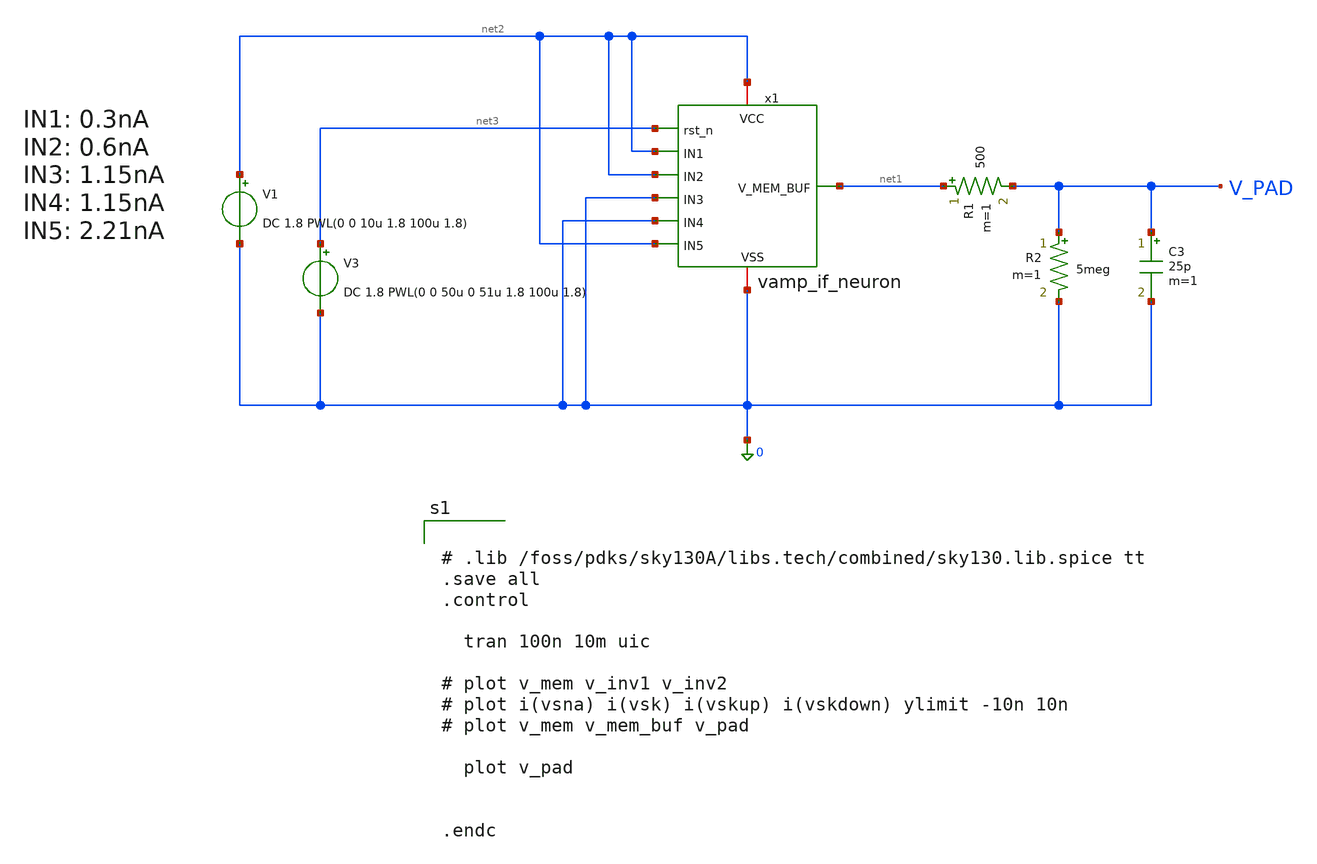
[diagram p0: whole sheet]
** sch_path: schem/vamp_if_neuron_tb.sch
**.subckt vamp_if_neuron_tb
V1 net2 0 DC 1.8 PWL(0 0 10u 1.8 100u 1.8)
V3 net3 0 DC 1.8 PWL(0 0 50u 0 51u 1.8 100u 1.8)
R1 net1 V_PAD 500 m=1
R2 V_PAD 0 5meg m=1
C3 V_PAD 0 25p m=1
x1 net2 net1 0 net3 net2 net2 0 0 net2 vamp_if_neuron
**** begin user architecture code


# .lib /foss/pdks/sky130A/libs.tech/combined/sky130.lib.spice tt
.save all
.control

  tran 100n 10m uic

# plot v_mem v_inv1 v_inv2
# plot i(vsna) i(vsk) i(vskup) i(vskdown) ylimit -10n 10n
# plot v_mem v_mem_buf v_pad

  plot v_pad


.endc



** opencircuitdesign pdks install
.lib $::SKYWATER_MODELS/sky130.lib.spice tt

**** end user architecture code
**.ends

* expanding   symbol:  vamp_if_neuron.sym # of pins=9
** sym_path: schem/vamp_if_neuron.sym
** sch_path: schem/vamp_if_neuron.sch
.subckt vamp_if_neuron VCC V_MEM_BUF VSS rst_n IN1 IN2 IN3 IN4 IN5
*.iopin VCC
*.iopin VSS
*.ipin rst_n
*.opin V_MEM_BUF
*.ipin IN1
*.ipin IN2
*.ipin IN3
*.ipin IN4
*.ipin IN5
x1 VCC net1 VSS VBN_REF10N V_MEM V_THRES ota
x2 VCC net1 V_inv1 VSS inv
XC1 V_MEM VSS sky130_fd_pr__cap_mim_m3_1 W=32 L=32 MF=1 m=1
XM1 net5 V_inv2 VK_SRC VSS sky130_fd_pr__nfet_01v8 L=4 W=1 nf=1 ad='int((1 + 1)/2) * 1 / 1 * 0.29' as='int((1 + 2)/2) * 1 / 1 * 0.29'
+ pd='2*int((1 + 1)/2) * (1 / 1 + 0.29)' ps='2*int((1 + 2)/2) * (1 / 1 + 0.29)' nrd='0.29 / 1 ' nrs='0.29 / 1 '
+ sa=0 sb=0 sd=0 mult=1 m=1
XM5 V_inv2 V_inv1 VNET_KDOWN_SRC VSS sky130_fd_pr__nfet_01v8 L=0.5 W=1 nf=1 ad='int((1 + 1)/2) * 1 / 1 * 0.29'
+ as='int((1 + 2)/2) * 1 / 1 * 0.29' pd='2*int((1 + 1)/2) * (1 / 1 + 0.29)' ps='2*int((1 + 2)/2) * (1 / 1 + 0.29)'
+ nrd='0.29 / 1 ' nrs='0.29 / 1 ' sa=0 sb=0 sd=0 mult=1 m=1
XM6 V_inv2 V_inv1 net3 VCC sky130_fd_pr__pfet_01v8_lvt L=0.5 W=2 nf=1 ad='int((1 + 1)/2) * 2 / 1 * 0.29'
+ as='int((1 + 2)/2) * 2 / 1 * 0.29' pd='2*int((1 + 1)/2) * (2 / 1 + 0.29)' ps='2*int((1 + 2)/2) * (2 / 1 + 0.29)'
+ nrd='0.29 / 2 ' nrs='0.29 / 2 ' sa=0 sb=0 sd=0 mult=1 m=1
XC2 V_inv2 VSS sky130_fd_pr__cap_mim_m3_1 W=35 L=35 MF=1 m=1
VSNA net6 V_MEM 0
.save i(vsna)
VSKUP net4 net3 0
.save i(vskup)
VSK net5 V_MEM 0
.save i(vsk)
VSKDOWN net2 VNET_KDOWN_SRC 0
.save i(vskdown)
XM2 VK_SRC VBN_REF10N VSS VSS sky130_fd_pr__nfet_01v8 L=4 W=1 nf=1 ad='int((1 + 1)/2) * 1 / 1 * 0.29'
+ as='int((1 + 2)/2) * 1 / 1 * 0.29' pd='2*int((1 + 1)/2) * (1 / 1 + 0.29)' ps='2*int((1 + 2)/2) * (1 / 1 + 0.29)'
+ nrd='0.29 / 1 ' nrs='0.29 / 1 ' sa=0 sb=0 sd=0 mult=4 m=4
XM3 net2 VBN_REF1N VSS VSS sky130_fd_pr__nfet_01v8 L=4 W=2 nf=1 ad='int((1 + 1)/2) * 2 / 1 * 0.29' as='int((1 + 2)/2) * 2 / 1 * 0.29'
+ pd='2*int((1 + 1)/2) * (2 / 1 + 0.29)' ps='2*int((1 + 2)/2) * (2 / 1 + 0.29)' nrd='0.29 / 2 ' nrs='0.29 / 2 '
+ sa=0 sb=0 sd=0 mult=1 m=1
XM7 VNA_SRC VBP_REF10N VCC VCC sky130_fd_pr__pfet_01v8 L=4 W=1 nf=1 ad='int((1 + 1)/2) * 1 / 1 * 0.29'
+ as='int((1 + 2)/2) * 1 / 1 * 0.29' pd='2*int((1 + 1)/2) * (1 / 1 + 0.29)' ps='2*int((1 + 2)/2) * (1 / 1 + 0.29)'
+ nrd='0.29 / 1 ' nrs='0.29 / 1 ' sa=0 sb=0 sd=0 mult=1 m=1
XM8 net4 VBP_REF1N VCC VCC sky130_fd_pr__pfet_01v8 L=4 W=2.5 nf=1 ad='int((1 + 1)/2) * 2.5 / 1 * 0.29'
+ as='int((1 + 2)/2) * 2.5 / 1 * 0.29' pd='2*int((1 + 1)/2) * (2.5 / 1 + 0.29)' ps='2*int((1 + 2)/2) * (2.5 / 1 + 0.29)'
+ nrd='0.29 / 2.5 ' nrs='0.29 / 2.5 ' sa=0 sb=0 sd=0 mult=2 m=2
XM4 net6 V_inv1 VNA_SRC VCC sky130_fd_pr__pfet_01v8_lvt L=4 W=2 nf=1 ad='int((1 + 1)/2) * 2 / 1 * 0.29'
+ as='int((1 + 2)/2) * 2 / 1 * 0.29' pd='2*int((1 + 1)/2) * (2 / 1 + 0.29)' ps='2*int((1 + 2)/2) * (2 / 1 + 0.29)'
+ nrd='0.29 / 2 ' nrs='0.29 / 2 ' sa=0 sb=0 sd=0 mult=1 m=1
VSIN V_STIM V_MEM 0
.save i(vsin)
x3 VCC VBP_REF10N VSS VBP_REF1N VBN_REF10N VBN_REF1N rst_n bmr
VSBUF net7 V_MEM_BUF 0
.save i(vsbuf)
XM9 VSS V_MEM V_MEM_BUF VCC sky130_fd_pr__pfet_01v8_lvt L=0.5 W=40 nf=1 ad='int((1 + 1)/2) * 40 / 1 * 0.29'
+ as='int((1 + 2)/2) * 40 / 1 * 0.29' pd='2*int((1 + 1)/2) * (40 / 1 + 0.29)' ps='2*int((1 + 2)/2) * (40 / 1 + 0.29)'
+ nrd='0.29 / 40 ' nrs='0.29 / 40 ' sa=0 sb=0 sd=0 mult=1 m=1
XM10 net7 VBP_REF10N VCC VCC sky130_fd_pr__pfet_01v8 L=0.75 W=10 nf=5 ad='int((5 + 1)/2) * 10 / 5 * 0.29'
+ as='int((5 + 2)/2) * 10 / 5 * 0.29' pd='2*int((5 + 1)/2) * (10 / 5 + 0.29)' ps='2*int((5 + 2)/2) * (10 / 5 + 0.29)'
+ nrd='0.29 / 10 ' nrs='0.29 / 10 ' sa=0 sb=0 sd=0 mult=2 m=2
XM11 net8 VBN_REF1N VSS VSS sky130_fd_pr__nfet_01v8 L=4 W=1 nf=1 ad='int((1 + 1)/2) * 1 / 1 * 0.29' as='int((1 + 2)/2) * 1 / 1 * 0.29'
+ pd='2*int((1 + 1)/2) * (1 / 1 + 0.29)' ps='2*int((1 + 2)/2) * (1 / 1 + 0.29)' nrd='0.29 / 1 ' nrs='0.29 / 1 '
+ sa=0 sb=0 sd=0 mult=1 m=1
VSLK net8 V_MEM 0
.save i(vslk)
X0.5 net9 VBP_REF1N VCC VCC sky130_fd_pr__pfet_01v8 L=16 W=0.5 nf=1 ad='int((1 + 1)/2) * 0.5 / 1 * 0.29'
+ as='int((1 + 2)/2) * 0.5 / 1 * 0.29' pd='2*int((1 + 1)/2) * (0.5 / 1 + 0.29)' ps='2*int((1 + 2)/2) * (0.5 / 1 + 0.29)'
+ nrd='0.29 / 0.5 ' nrs='0.29 / 0.5 ' sa=0 sb=0 sd=0 mult=1 m=1
XM13 V_STIM IN1 net9 VCC sky130_fd_pr__pfet_01v8_lvt L=4 W=2 nf=1 ad='int((1 + 1)/2) * 2 / 1 * 0.29'
+ as='int((1 + 2)/2) * 2 / 1 * 0.29' pd='2*int((1 + 1)/2) * (2 / 1 + 0.29)' ps='2*int((1 + 2)/2) * (2 / 1 + 0.29)'
+ nrd='0.29 / 2 ' nrs='0.29 / 2 ' sa=0 sb=0 sd=0 mult=1 m=1
XM14 net10 VBP_REF1N VCC VCC sky130_fd_pr__pfet_01v8 L=8 W=0.5 nf=1 ad='int((1 + 1)/2) * 0.5 / 1 * 0.29'
+ as='int((1 + 2)/2) * 0.5 / 1 * 0.29' pd='2*int((1 + 1)/2) * (0.5 / 1 + 0.29)' ps='2*int((1 + 2)/2) * (0.5 / 1 + 0.29)'
+ nrd='0.29 / 0.5 ' nrs='0.29 / 0.5 ' sa=0 sb=0 sd=0 mult=1 m=1
XM15 V_STIM IN2 net10 VCC sky130_fd_pr__pfet_01v8_lvt L=4 W=2 nf=1 ad='int((1 + 1)/2) * 2 / 1 * 0.29'
+ as='int((1 + 2)/2) * 2 / 1 * 0.29' pd='2*int((1 + 1)/2) * (2 / 1 + 0.29)' ps='2*int((1 + 2)/2) * (2 / 1 + 0.29)'
+ nrd='0.29 / 2 ' nrs='0.29 / 2 ' sa=0 sb=0 sd=0 mult=1 m=1
XM16 net11 VBP_REF1N VCC VCC sky130_fd_pr__pfet_01v8 L=4 W=1 nf=1 ad='int((1 + 1)/2) * 1 / 1 * 0.29'
+ as='int((1 + 2)/2) * 1 / 1 * 0.29' pd='2*int((1 + 1)/2) * (1 / 1 + 0.29)' ps='2*int((1 + 2)/2) * (1 / 1 + 0.29)'
+ nrd='0.29 / 1 ' nrs='0.29 / 1 ' sa=0 sb=0 sd=0 mult=1 m=1
XM17 V_STIM IN3 net11 VCC sky130_fd_pr__pfet_01v8_lvt L=4 W=2 nf=1 ad='int((1 + 1)/2) * 2 / 1 * 0.29'
+ as='int((1 + 2)/2) * 2 / 1 * 0.29' pd='2*int((1 + 1)/2) * (2 / 1 + 0.29)' ps='2*int((1 + 2)/2) * (2 / 1 + 0.29)'
+ nrd='0.29 / 2 ' nrs='0.29 / 2 ' sa=0 sb=0 sd=0 mult=1 m=1
XM18 net12 VBP_REF1N VCC VCC sky130_fd_pr__pfet_01v8 L=4 W=1 nf=1 ad='int((1 + 1)/2) * 1 / 1 * 0.29'
+ as='int((1 + 2)/2) * 1 / 1 * 0.29' pd='2*int((1 + 1)/2) * (1 / 1 + 0.29)' ps='2*int((1 + 2)/2) * (1 / 1 + 0.29)'
+ nrd='0.29 / 1 ' nrs='0.29 / 1 ' sa=0 sb=0 sd=0 mult=1 m=1
XM19 V_STIM IN4 net12 VCC sky130_fd_pr__pfet_01v8_lvt L=4 W=2 nf=1 ad='int((1 + 1)/2) * 2 / 1 * 0.29'
+ as='int((1 + 2)/2) * 2 / 1 * 0.29' pd='2*int((1 + 1)/2) * (2 / 1 + 0.29)' ps='2*int((1 + 2)/2) * (2 / 1 + 0.29)'
+ nrd='0.29 / 2 ' nrs='0.29 / 2 ' sa=0 sb=0 sd=0 mult=1 m=1
XM20 net13 VBP_REF1N VCC VCC sky130_fd_pr__pfet_01v8 L=4 W=1 nf=1 ad='int((1 + 1)/2) * 1 / 1 * 0.29'
+ as='int((1 + 2)/2) * 1 / 1 * 0.29' pd='2*int((1 + 1)/2) * (1 / 1 + 0.29)' ps='2*int((1 + 2)/2) * (1 / 1 + 0.29)'
+ nrd='0.29 / 1 ' nrs='0.29 / 1 ' sa=0 sb=0 sd=0 mult=2 m=2
XM21 V_STIM IN5 net13 VCC sky130_fd_pr__pfet_01v8_lvt L=4 W=2 nf=1 ad='int((1 + 1)/2) * 2 / 1 * 0.29'
+ as='int((1 + 2)/2) * 2 / 1 * 0.29' pd='2*int((1 + 1)/2) * (2 / 1 + 0.29)' ps='2*int((1 + 2)/2) * (2 / 1 + 0.29)'
+ nrd='0.29 / 2 ' nrs='0.29 / 2 ' sa=0 sb=0 sd=0 mult=1 m=1
XR3 V_THRES VCC VSS sky130_fd_pr__res_xhigh_po_0p35 L=10 mult=1 m=1
XR4 VSS V_THRES VSS sky130_fd_pr__res_xhigh_po_0p35 L=6.36 mult=1 m=1
.ends


* expanding   symbol:  ota/ota.sym # of pins=6
** sym_path: schem/ota/ota.sym
** sch_path: schem/ota/ota.sch
.subckt ota VCC OUT VSS BIAS + -
*.ipin BIAS
*.ipin +
*.ipin -
*.opin OUT
*.iopin VCC
*.iopin VSS
XM1 VSRC + VBOT VSS sky130_fd_pr__nfet_01v8 L=0.5 W=1 nf=1 ad='int((1 + 1)/2) * 1 / 1 * 0.29' as='int((1 + 2)/2) * 1 / 1 * 0.29'
+ pd='2*int((1 + 1)/2) * (1 / 1 + 0.29)' ps='2*int((1 + 2)/2) * (1 / 1 + 0.29)' nrd='0.29 / 1 ' nrs='0.29 / 1 '
+ sa=0 sb=0 sd=0 mult=1 m=1
XM2 OUT - VBOT VSS sky130_fd_pr__nfet_01v8 L=0.5 W=1 nf=1 ad='int((1 + 1)/2) * 1 / 1 * 0.29' as='int((1 + 2)/2) * 1 / 1 * 0.29'
+ pd='2*int((1 + 1)/2) * (1 / 1 + 0.29)' ps='2*int((1 + 2)/2) * (1 / 1 + 0.29)' nrd='0.29 / 1 ' nrs='0.29 / 1 '
+ sa=0 sb=0 sd=0 mult=1 m=1
XM3 VSRC VSRC VCC VCC sky130_fd_pr__pfet_01v8_lvt L=0.5 W=2 nf=1 ad='int((1 + 1)/2) * 2 / 1 * 0.29' as='int((1 + 2)/2) * 2 / 1 * 0.29'
+ pd='2*int((1 + 1)/2) * (2 / 1 + 0.29)' ps='2*int((1 + 2)/2) * (2 / 1 + 0.29)' nrd='0.29 / 2 ' nrs='0.29 / 2 '
+ sa=0 sb=0 sd=0 mult=1 m=1
XM4 OUT VSRC VCC VCC sky130_fd_pr__pfet_01v8_lvt L=0.5 W=2 nf=1 ad='int((1 + 1)/2) * 2 / 1 * 0.29' as='int((1 + 2)/2) * 2 / 1 * 0.29'
+ pd='2*int((1 + 1)/2) * (2 / 1 + 0.29)' ps='2*int((1 + 2)/2) * (2 / 1 + 0.29)' nrd='0.29 / 2 ' nrs='0.29 / 2 '
+ sa=0 sb=0 sd=0 mult=1 m=1
XM5 VBOT BIAS VSS VSS sky130_fd_pr__nfet_01v8 L=0.5 W=1 nf=1 ad='int((1 + 1)/2) * 1 / 1 * 0.29' as='int((1 + 2)/2) * 1 / 1 * 0.29'
+ pd='2*int((1 + 1)/2) * (1 / 1 + 0.29)' ps='2*int((1 + 2)/2) * (1 / 1 + 0.29)' nrd='0.29 / 1 ' nrs='0.29 / 1 '
+ sa=0 sb=0 sd=0 mult=1 m=1
.ends


* expanding   symbol:  inv/inv.sym # of pins=4
** sym_path: schem/inv/inv.sym
** sch_path: schem/inv/inv.sch
.subckt inv VDD IN OUT VSS
*.ipin IN
*.iopin VDD
*.iopin VSS
*.opin OUT
XM1 OUT IN VSS VSS sky130_fd_pr__nfet_01v8 L=0.5 W=1 nf=1 ad='int((1 + 1)/2) * 1 / 1 * 0.29' as='int((1 + 2)/2) * 1 / 1 * 0.29'
+ pd='2*int((1 + 1)/2) * (1 / 1 + 0.29)' ps='2*int((1 + 2)/2) * (1 / 1 + 0.29)' nrd='0.29 / 1 ' nrs='0.29 / 1 '
+ sa=0 sb=0 sd=0 mult=1 m=1
XM2 OUT IN VDD VDD sky130_fd_pr__pfet_01v8_lvt L=0.5 W=2 nf=1 ad='int((1 + 1)/2) * 2 / 1 * 0.29' as='int((1 + 2)/2) * 2 / 1 * 0.29'
+ pd='2*int((1 + 1)/2) * (2 / 1 + 0.29)' ps='2*int((1 + 2)/2) * (2 / 1 + 0.29)' nrd='0.29 / 2 ' nrs='0.29 / 2 '
+ sa=0 sb=0 sd=0 mult=1 m=1
.ends


* expanding   symbol:  bias/bmr.sym # of pins=7
** sym_path: schem/bias/bmr.sym
** sch_path: schem/bias/bmr.sch
.subckt bmr VCC VBP_REF10N VSS VBP_REF1N VBN_REF10N VBN_REF1N rst_n
*.iopin VCC
*.iopin VSS
*.ipin rst_n
*.opin VBP_REF10N
*.opin VBP_REF1N
*.opin VBN_REF10N
*.opin VBN_REF1N
x1 VCC VBP_REF10N VSS VBN_REF10N rst_n bmr_10n
XM1 net1 VBP_REF10N VCC VCC sky130_fd_pr__pfet_01v8 L=4 W=1 nf=1 ad='int((1 + 1)/2) * 1 / 1 * 0.29' as='int((1 + 2)/2) * 1 / 1 * 0.29'
+ pd='2*int((1 + 1)/2) * (1 / 1 + 0.29)' ps='2*int((1 + 2)/2) * (1 / 1 + 0.29)' nrd='0.29 / 1 ' nrs='0.29 / 1 '
+ sa=0 sb=0 sd=0 mult=1 m=1
XM2 VBN_REF1N VBN_REF1N VSS VSS sky130_fd_pr__nfet_01v8 L=4 W=1 nf=1 ad='int((1 + 1)/2) * 1 / 1 * 0.29'
+ as='int((1 + 2)/2) * 1 / 1 * 0.29' pd='2*int((1 + 1)/2) * (1 / 1 + 0.29)' ps='2*int((1 + 2)/2) * (1 / 1 + 0.29)'
+ nrd='0.29 / 1 ' nrs='0.29 / 1 ' sa=0 sb=0 sd=0 mult=10 m=10
XM3 net2 VBN_REF1N VSS VSS sky130_fd_pr__nfet_01v8 L=4 W=1 nf=1 ad='int((1 + 1)/2) * 1 / 1 * 0.29' as='int((1 + 2)/2) * 1 / 1 * 0.29'
+ pd='2*int((1 + 1)/2) * (1 / 1 + 0.29)' ps='2*int((1 + 2)/2) * (1 / 1 + 0.29)' nrd='0.29 / 1 ' nrs='0.29 / 1 '
+ sa=0 sb=0 sd=0 mult=1 m=1
XM4 VBP_REF1N VBP_REF1N VCC VCC sky130_fd_pr__pfet_01v8 L=4 W=1 nf=1 ad='int((1 + 1)/2) * 1 / 1 * 0.29'
+ as='int((1 + 2)/2) * 1 / 1 * 0.29' pd='2*int((1 + 1)/2) * (1 / 1 + 0.29)' ps='2*int((1 + 2)/2) * (1 / 1 + 0.29)'
+ nrd='0.29 / 1 ' nrs='0.29 / 1 ' sa=0 sb=0 sd=0 mult=1 m=1
Vmeas net1 VBN_REF1N 0
.save i(vmeas)
Vmeas1 VBP_REF1N net2 0
.save i(vmeas1)
.ends


* expanding   symbol:  bias/bmr_10n.sym # of pins=5
** sym_path: schem/bias/bmr_10n.sym
** sch_path: schem/bias/bmr_10n.sch
.subckt bmr_10n VCC VBP VSS VBN rst_n
*.iopin VCC
*.iopin VSS
*.ipin rst_n
*.opin VBP
*.opin VBN
XM1 VBP VBP VCC VCC sky130_fd_pr__pfet_01v8 L=4 W=1 nf=1 ad='int((1 + 1)/2) * 1 / 1 * 0.29' as='int((1 + 2)/2) * 1 / 1 * 0.29'
+ pd='2*int((1 + 1)/2) * (1 / 1 + 0.29)' ps='2*int((1 + 2)/2) * (1 / 1 + 0.29)' nrd='0.29 / 1 ' nrs='0.29 / 1 '
+ sa=0 sb=0 sd=0 mult=1 m=1
XM2 net3 VBP VCC VCC sky130_fd_pr__pfet_01v8 L=4 W=1 nf=1 ad='int((1 + 1)/2) * 1 / 1 * 0.29' as='int((1 + 2)/2) * 1 / 1 * 0.29'
+ pd='2*int((1 + 1)/2) * (1 / 1 + 0.29)' ps='2*int((1 + 2)/2) * (1 / 1 + 0.29)' nrd='0.29 / 1 ' nrs='0.29 / 1 '
+ sa=0 sb=0 sd=0 mult=1 m=1
XM3 net2 VBN net1 VSS sky130_fd_pr__nfet_01v8 L=4 W=8 nf=1 ad='int((1 + 1)/2) * 8 / 1 * 0.29' as='int((1 + 2)/2) * 8 / 1 * 0.29'
+ pd='2*int((1 + 1)/2) * (8 / 1 + 0.29)' ps='2*int((1 + 2)/2) * (8 / 1 + 0.29)' nrd='0.29 / 8 ' nrs='0.29 / 8 '
+ sa=0 sb=0 sd=0 mult=1 m=1
XM4 VBN VBN VSS VSS sky130_fd_pr__nfet_01v8 L=4 W=1 nf=1 ad='int((1 + 1)/2) * 1 / 1 * 0.29' as='int((1 + 2)/2) * 1 / 1 * 0.29'
+ pd='2*int((1 + 1)/2) * (1 / 1 + 0.29)' ps='2*int((1 + 2)/2) * (1 / 1 + 0.29)' nrd='0.29 / 1 ' nrs='0.29 / 1 '
+ sa=0 sb=0 sd=0 mult=1 m=1
XR1 net5 net1 net4 sky130_fd_pr__res_xhigh_po_0p35 L={LR} mult=1 m=1
VSRIGHT VBP net2 0
.save i(vsright)
VSLEFT net3 VBN 0
.save i(vsleft)
XM5 VBN rst_n VCC VCC sky130_fd_pr__pfet_01v8 L=4 W=1 nf=1 ad='int((1 + 1)/2) * 1 / 1 * 0.29' as='int((1 + 2)/2) * 1 / 1 * 0.29'
+ pd='2*int((1 + 1)/2) * (1 / 1 + 0.29)' ps='2*int((1 + 2)/2) * (1 / 1 + 0.29)' nrd='0.29 / 1 ' nrs='0.29 / 1 '
+ sa=0 sb=0 sd=0 mult=1 m=1
XR2 net6 net5 net4 sky130_fd_pr__res_xhigh_po_0p35 L={LR} mult=1 m=1
XR3 net7 net6 net4 sky130_fd_pr__res_xhigh_po_0p35 L={LR} mult=1 m=1
XR4 net8 net7 net4 sky130_fd_pr__res_xhigh_po_0p35 L={LR} mult=1 m=1
XR5 net9 net8 net4 sky130_fd_pr__res_xhigh_po_0p35 L={LR} mult=1 m=1
XR6 net10 net9 net4 sky130_fd_pr__res_xhigh_po_0p35 L={LR} mult=1 m=1
XR7 net11 net10 net4 sky130_fd_pr__res_xhigh_po_0p35 L={LR} mult=1 m=1
XR8 VSS net11 net4 sky130_fd_pr__res_xhigh_po_0p35 L={LR} mult=1 m=1
**** begin user architecture code


.param LR=1084/8


**** end user architecture code
.ends

.end
